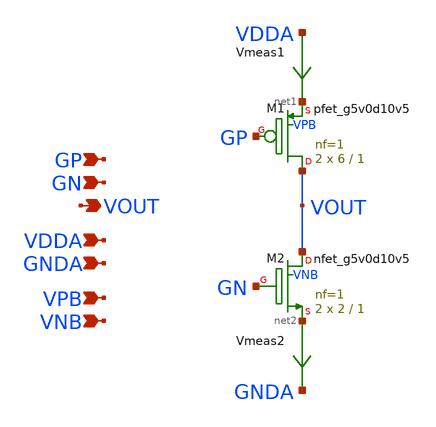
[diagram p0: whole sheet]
** sch_path: xschem/output_stage.sch
**.subckt output_stage GP GN VOUT VDDA VPB GNDA VNB
*.ipin GP
*.ipin GN
*.opin VOUT
*.ipin VDDA
*.ipin VPB
*.ipin GNDA
*.ipin VNB
XM1 VOUT GP net1 VPB sky130_fd_pr__pfet_g5v0d10v5 L=1 W=6 nf=1 ad='int((nf+1)/2) * W/nf * 0.29' as='int((nf+2)/2) * W/nf * 0.29'
+ pd='2*int((nf+1)/2) * (W/nf + 0.29)' ps='2*int((nf+2)/2) * (W/nf + 0.29)' nrd='0.29 / W' nrs='0.29 / W'
+ sa=0 sb=0 sd=0 mult=2 m=2
XM2 VOUT GN net2 VNB sky130_fd_pr__nfet_g5v0d10v5 L=1 W=2 nf=1 ad='int((nf+1)/2) * W/nf * 0.29' as='int((nf+2)/2) * W/nf * 0.29'
+ pd='2*int((nf+1)/2) * (W/nf + 0.29)' ps='2*int((nf+2)/2) * (W/nf + 0.29)' nrd='0.29 / W' nrs='0.29 / W'
+ sa=0 sb=0 sd=0 mult=2 m=2
Vmeas1 VDDA net1 0
.save i(vmeas1)
Vmeas2 net2 GNDA 0
.save i(vmeas2)
**.ends
.end
